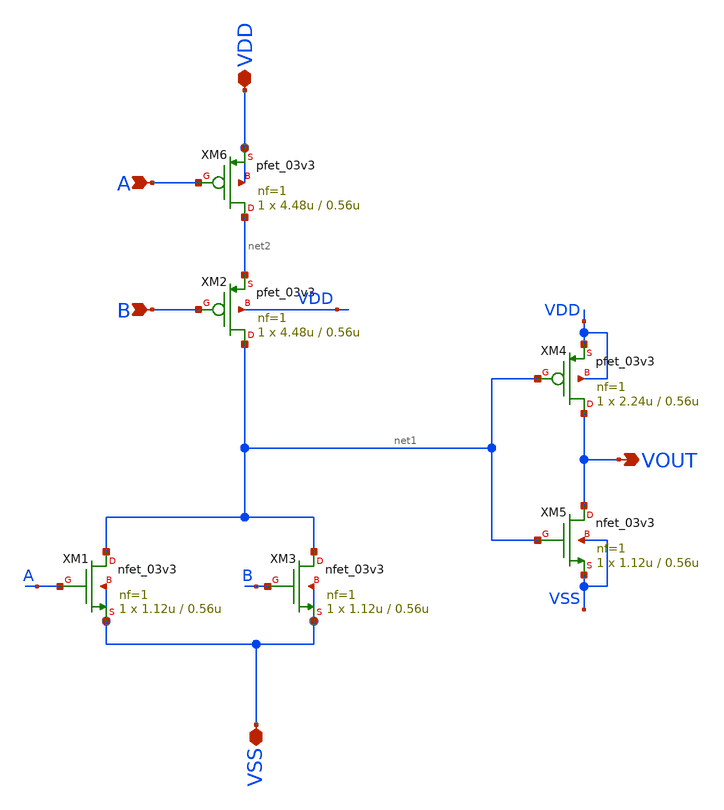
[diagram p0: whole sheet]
** sch_path: PLL-main/schematic/xschem/OR.sch
**.subckt OR VSS VDD A B VOUT
*.iopin VSS
*.iopin VDD
*.ipin A
*.ipin B
*.opin VOUT
XM1 net1 A VSS VSS nfet_03v3 L=0.56u W=1.12u nf=1 ad='int((nf+1)/2) * W/nf * 0.18u' as='int((nf+2)/2) * W/nf * 0.18u'
+ pd='2*int((nf+1)/2) * (W/nf + 0.18u)' ps='2*int((nf+2)/2) * (W/nf + 0.18u)' nrd='0.18u / W' nrs='0.18u / W'
+ sa=0 sb=0 sd=0 m=1
XM2 net1 B net2 VDD pfet_03v3 L=0.56u W=4.48u nf=1 ad='int((nf+1)/2) * W/nf * 0.18u' as='int((nf+2)/2) * W/nf * 0.18u'
+ pd='2*int((nf+1)/2) * (W/nf + 0.18u)' ps='2*int((nf+2)/2) * (W/nf + 0.18u)' nrd='0.18u / W' nrs='0.18u / W'
+ sa=0 sb=0 sd=0 m=1
XM3 net1 B VSS VSS nfet_03v3 L=0.56u W=1.12u nf=1 ad='int((nf+1)/2) * W/nf * 0.18u' as='int((nf+2)/2) * W/nf * 0.18u'
+ pd='2*int((nf+1)/2) * (W/nf + 0.18u)' ps='2*int((nf+2)/2) * (W/nf + 0.18u)' nrd='0.18u / W' nrs='0.18u / W'
+ sa=0 sb=0 sd=0 m=1
XM6 net2 A VDD VDD pfet_03v3 L=0.56u W=4.48u nf=1 ad='int((nf+1)/2) * W/nf * 0.18u' as='int((nf+2)/2) * W/nf * 0.18u'
+ pd='2*int((nf+1)/2) * (W/nf + 0.18u)' ps='2*int((nf+2)/2) * (W/nf + 0.18u)' nrd='0.18u / W' nrs='0.18u / W'
+ sa=0 sb=0 sd=0 m=1
XM4 VOUT net1 VDD VDD pfet_03v3 L=0.56u W=2.24u nf=1 ad='int((nf+1)/2) * W/nf * 0.18u' as='int((nf+2)/2) * W/nf * 0.18u'
+ pd='2*int((nf+1)/2) * (W/nf + 0.18u)' ps='2*int((nf+2)/2) * (W/nf + 0.18u)' nrd='0.18u / W' nrs='0.18u / W'
+ sa=0 sb=0 sd=0 m=1
XM5 VOUT net1 VSS VSS nfet_03v3 L=0.56u W=1.12u nf=1 ad='int((nf+1)/2) * W/nf * 0.18u' as='int((nf+2)/2) * W/nf * 0.18u'
+ pd='2*int((nf+1)/2) * (W/nf + 0.18u)' ps='2*int((nf+2)/2) * (W/nf + 0.18u)' nrd='0.18u / W' nrs='0.18u / W'
+ sa=0 sb=0 sd=0 m=1
**.ends
.end
